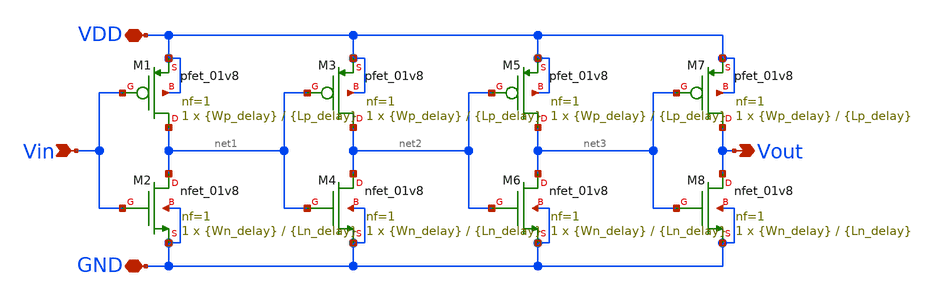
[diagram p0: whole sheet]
** sch_path: SNN/Delay_Circuit.sch
**.subckt Delay_Circuit Vin Vout VDD GND
*.ipin Vin
*.opin Vout
*.iopin VDD
*.iopin GND
XM1 net1 Vin VDD VDD sky130_fd_pr__pfet_01v8 L={Lp_delay} W={Wp_delay} nf=1 ad='int((nf+1)/2) * W/nf * 0.29'
+ as='int((nf+2)/2) * W/nf * 0.29' pd='2*int((nf+1)/2) * (W/nf + 0.29)' ps='2*int((nf+2)/2) * (W/nf + 0.29)'
+ nrd='0.29 / W' nrs='0.29 / W' sa=0 sb=0 sd=0 mult=1 m=1
XM2 net1 Vin GND GND sky130_fd_pr__nfet_01v8 L={Ln_delay} W={Wn_delay} nf=1 ad='int((nf+1)/2) * W/nf * 0.29'
+ as='int((nf+2)/2) * W/nf * 0.29' pd='2*int((nf+1)/2) * (W/nf + 0.29)' ps='2*int((nf+2)/2) * (W/nf + 0.29)'
+ nrd='0.29 / W' nrs='0.29 / W' sa=0 sb=0 sd=0 mult=1 m=1
XM3 net2 net1 VDD VDD sky130_fd_pr__pfet_01v8 L={Lp_delay} W={Wp_delay} nf=1 ad='int((nf+1)/2) * W/nf * 0.29'
+ as='int((nf+2)/2) * W/nf * 0.29' pd='2*int((nf+1)/2) * (W/nf + 0.29)' ps='2*int((nf+2)/2) * (W/nf + 0.29)'
+ nrd='0.29 / W' nrs='0.29 / W' sa=0 sb=0 sd=0 mult=1 m=1
XM4 net2 net1 GND GND sky130_fd_pr__nfet_01v8 L={Ln_delay} W={Wn_delay} nf=1 ad='int((nf+1)/2) * W/nf * 0.29'
+ as='int((nf+2)/2) * W/nf * 0.29' pd='2*int((nf+1)/2) * (W/nf + 0.29)' ps='2*int((nf+2)/2) * (W/nf + 0.29)'
+ nrd='0.29 / W' nrs='0.29 / W' sa=0 sb=0 sd=0 mult=1 m=1
XM5 net3 net2 VDD VDD sky130_fd_pr__pfet_01v8 L={Lp_delay} W={Wp_delay} nf=1 ad='int((nf+1)/2) * W/nf * 0.29'
+ as='int((nf+2)/2) * W/nf * 0.29' pd='2*int((nf+1)/2) * (W/nf + 0.29)' ps='2*int((nf+2)/2) * (W/nf + 0.29)'
+ nrd='0.29 / W' nrs='0.29 / W' sa=0 sb=0 sd=0 mult=1 m=1
XM6 net3 net2 GND GND sky130_fd_pr__nfet_01v8 L={Ln_delay} W={Wn_delay} nf=1 ad='int((nf+1)/2) * W/nf * 0.29'
+ as='int((nf+2)/2) * W/nf * 0.29' pd='2*int((nf+1)/2) * (W/nf + 0.29)' ps='2*int((nf+2)/2) * (W/nf + 0.29)'
+ nrd='0.29 / W' nrs='0.29 / W' sa=0 sb=0 sd=0 mult=1 m=1
XM7 Vout net3 VDD VDD sky130_fd_pr__pfet_01v8 L={Lp_delay} W={Wp_delay} nf=1 ad='int((nf+1)/2) * W/nf * 0.29'
+ as='int((nf+2)/2) * W/nf * 0.29' pd='2*int((nf+1)/2) * (W/nf + 0.29)' ps='2*int((nf+2)/2) * (W/nf + 0.29)'
+ nrd='0.29 / W' nrs='0.29 / W' sa=0 sb=0 sd=0 mult=1 m=1
XM8 Vout net3 GND GND sky130_fd_pr__nfet_01v8 L={Ln_delay} W={Wn_delay} nf=1 ad='int((nf+1)/2) * W/nf * 0.29'
+ as='int((nf+2)/2) * W/nf * 0.29' pd='2*int((nf+1)/2) * (W/nf + 0.29)' ps='2*int((nf+2)/2) * (W/nf + 0.29)'
+ nrd='0.29 / W' nrs='0.29 / W' sa=0 sb=0 sd=0 mult=1 m=1
**.ends
.end
